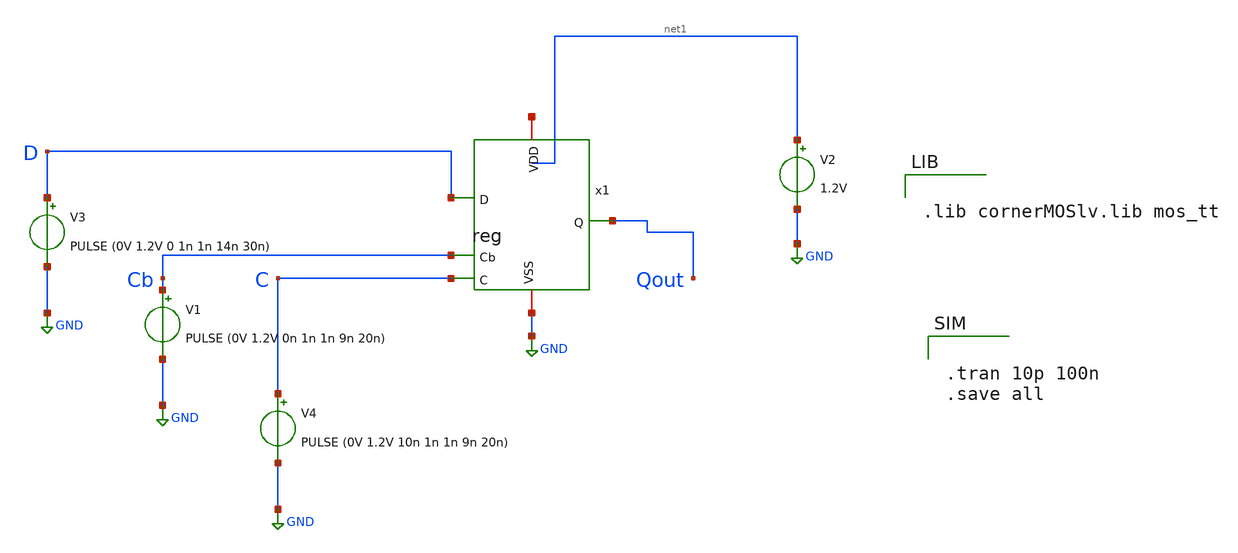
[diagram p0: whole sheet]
** sch_path: reg-testbench.sch
**.subckt reg-testbench
V2 net1 GND 1.2V
V3 D GND PULSE (0V 1.2V 0 1n 1n 14n 30n)
V1 Cb GND PULSE (0V 1.2V 0n 1n 1n 9n 20n)
V4 C GND PULSE (0V 1.2V 10n 1n 1n 9n 20n)
x1 net2 D Qout Cb C GND reg
**** begin user architecture code


.tran 10p 100n
.save all




.lib cornerMOSlv.lib mos_tt

**** end user architecture code
**.ends

* expanding   symbol:  xchem/xchem/reg.sym # of pins=6
** sym_path: reg.sym
** sch_path: reg.sch
.subckt reg VDD D Q Cb C VSS
*.ipin C
*.ipin Cb
*.ipin D
*.opin Q
*.iopin VDD
*.iopin VSS
x1 VDD Cb C D net1 VSS dlatch
x2 VDD C Cb net1 Q VSS dlatch
.ends


* expanding   symbol:  xchem/xchem/dlatch.sym # of pins=6
** sym_path: dlatch.sym
** sch_path: dlatch.sch
.subckt dlatch VDD C Cb D Q VSS
*.ipin C
*.ipin Cb
*.ipin D
*.opin Q
*.iopin VDD
*.iopin VSS
x1 VDD net2 net1 C Cb VSS D mux
x2 VDD net1 Q VSS inverter
x3 VDD Q net2 VSS inverter
.ends


* expanding   symbol:  xchem/xchem/mux.sym # of pins=7
** sym_path: mux.sym
** sch_path: mux.sch
.subckt mux VDD D1 Y S Sb VSS D0
*.ipin S
*.ipin Sb
*.ipin D0
*.ipin D1
*.iopin VDD
*.iopin VSS
*.iopin Y
XM1 Y Sb D1 VDD sg13_lv_pmos w=0.15u l=0.13u ng=1 m=1 mm_ok=1
XM2 D0 S Y VDD sg13_lv_pmos w=0.15u l=0.13u ng=1 m=1 mm_ok=1
XM3 Y S D1 VSS sg13_lv_nmos w=0.15u l=0.13u ng=1 m=1 mm_ok=1
XM4 D0 Sb Y VSS sg13_lv_nmos w=0.15u l=0.13u ng=1 m=1 mm_ok=1
.ends


* expanding   symbol:  xchem/xchem/inverter.sym # of pins=4
** sym_path: inverter.sym
** sch_path: inverter.sch
.subckt inverter VDD A Y VSS
*.ipin A
*.iopin VDD
*.iopin VSS
*.opin Y
XM1 Y A VDD VDD sg13_lv_pmos w=0.15u l=0.13u ng=1 m=1 mm_ok=1
XM2 Y A VSS VSS sg13_lv_nmos w=0.15u l=0.13u ng=1 m=1 mm_ok=1
.ends

.GLOBAL GND
.end
